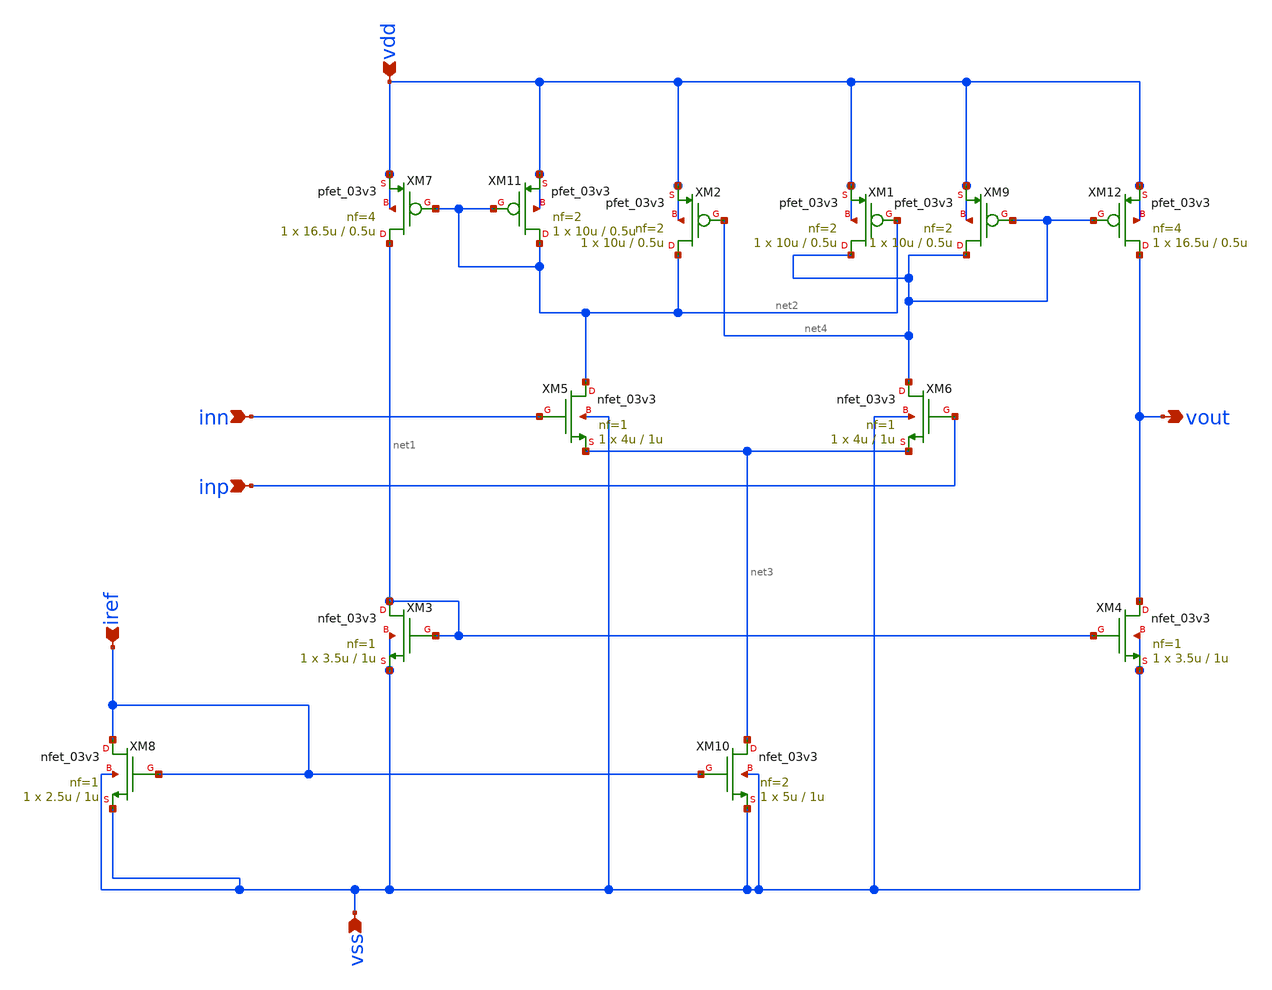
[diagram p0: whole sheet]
** sch_path: designs/libs/core_analog/Comparator/Nmos_Comparator.sch
**.subckt Nmos_Comparator vss vdd iref inn inp vout
*.ipin vss
*.ipin vdd
*.ipin iref
*.ipin inn
*.ipin inp
*.opin vout
XM3 net1 net1 vss vss nfet_03v3 L=1u W=3.5u nf=1 ad='int((nf+1)/2) * W/nf * 0.18u' as='int((nf+2)/2) * W/nf * 0.18u'
+ pd='2*int((nf+1)/2) * (W/nf + 0.18u)' ps='2*int((nf+2)/2) * (W/nf + 0.18u)' nrd='0.18u / W' nrs='0.18u / W'
+ sa=0 sb=0 sd=0 m=1
XM4 vout net1 vss vss nfet_03v3 L=1u W=3.5u nf=1 ad='int((nf+1)/2) * W/nf * 0.18u' as='int((nf+2)/2) * W/nf * 0.18u'
+ pd='2*int((nf+1)/2) * (W/nf + 0.18u)' ps='2*int((nf+2)/2) * (W/nf + 0.18u)' nrd='0.18u / W' nrs='0.18u / W'
+ sa=0 sb=0 sd=0 m=1
XM5 net2 inn net3 vss nfet_03v3 L=1u W=4u nf=1 ad='int((nf+1)/2) * W/nf * 0.18u' as='int((nf+2)/2) * W/nf * 0.18u'
+ pd='2*int((nf+1)/2) * (W/nf + 0.18u)' ps='2*int((nf+2)/2) * (W/nf + 0.18u)' nrd='0.18u / W' nrs='0.18u / W'
+ sa=0 sb=0 sd=0 m=1
XM6 net4 inp net3 vss nfet_03v3 L=1u W=4u nf=1 ad='int((nf+1)/2) * W/nf * 0.18u' as='int((nf+2)/2) * W/nf * 0.18u'
+ pd='2*int((nf+1)/2) * (W/nf + 0.18u)' ps='2*int((nf+2)/2) * (W/nf + 0.18u)' nrd='0.18u / W' nrs='0.18u / W'
+ sa=0 sb=0 sd=0 m=1
XM7 net1 net2 vdd vdd pfet_03v3 L=0.5u W=16.5u nf=4 ad='int((nf+1)/2) * W/nf * 0.18u' as='int((nf+2)/2) * W/nf * 0.18u'
+ pd='2*int((nf+1)/2) * (W/nf + 0.18u)' ps='2*int((nf+2)/2) * (W/nf + 0.18u)' nrd='0.18u / W' nrs='0.18u / W'
+ sa=0 sb=0 sd=0 m=1
XM9 net4 net4 vdd vdd pfet_03v3 L=0.5u W=10u nf=2 ad='int((nf+1)/2) * W/nf * 0.18u' as='int((nf+2)/2) * W/nf * 0.18u'
+ pd='2*int((nf+1)/2) * (W/nf + 0.18u)' ps='2*int((nf+2)/2) * (W/nf + 0.18u)' nrd='0.18u / W' nrs='0.18u / W'
+ sa=0 sb=0 sd=0 m=1
XM11 net2 net2 vdd vdd pfet_03v3 L=0.5u W=10u nf=2 ad='int((nf+1)/2) * W/nf * 0.18u' as='int((nf+2)/2) * W/nf * 0.18u'
+ pd='2*int((nf+1)/2) * (W/nf + 0.18u)' ps='2*int((nf+2)/2) * (W/nf + 0.18u)' nrd='0.18u / W' nrs='0.18u / W'
+ sa=0 sb=0 sd=0 m=1
XM12 vout net4 vdd vdd pfet_03v3 L=0.5u W=16.5u nf=4 ad='int((nf+1)/2) * W/nf * 0.18u' as='int((nf+2)/2) * W/nf * 0.18u'
+ pd='2*int((nf+1)/2) * (W/nf + 0.18u)' ps='2*int((nf+2)/2) * (W/nf + 0.18u)' nrd='0.18u / W' nrs='0.18u / W'
+ sa=0 sb=0 sd=0 m=1
XM1 net4 net2 vdd vdd pfet_03v3 L=0.5u W=10u nf=2 ad='int((nf+1)/2) * W/nf * 0.18u' as='int((nf+2)/2) * W/nf * 0.18u'
+ pd='2*int((nf+1)/2) * (W/nf + 0.18u)' ps='2*int((nf+2)/2) * (W/nf + 0.18u)' nrd='0.18u / W' nrs='0.18u / W'
+ sa=0 sb=0 sd=0 m=1
XM2 net2 net4 vdd vdd pfet_03v3 L=0.5u W=10u nf=2 ad='int((nf+1)/2) * W/nf * 0.18u' as='int((nf+2)/2) * W/nf * 0.18u'
+ pd='2*int((nf+1)/2) * (W/nf + 0.18u)' ps='2*int((nf+2)/2) * (W/nf + 0.18u)' nrd='0.18u / W' nrs='0.18u / W'
+ sa=0 sb=0 sd=0 m=1
XM8 iref iref vss vss nfet_03v3 L=1u W=2.5u nf=1 ad='int((nf+1)/2) * W/nf * 0.18u' as='int((nf+2)/2) * W/nf * 0.18u'
+ pd='2*int((nf+1)/2) * (W/nf + 0.18u)' ps='2*int((nf+2)/2) * (W/nf + 0.18u)' nrd='0.18u / W' nrs='0.18u / W'
+ sa=0 sb=0 sd=0 m=1
XM10 net3 iref vss vss nfet_03v3 L=1u W=5u nf=2 ad='int((nf+1)/2) * W/nf * 0.18u' as='int((nf+2)/2) * W/nf * 0.18u'
+ pd='2*int((nf+1)/2) * (W/nf + 0.18u)' ps='2*int((nf+2)/2) * (W/nf + 0.18u)' nrd='0.18u / W' nrs='0.18u / W'
+ sa=0 sb=0 sd=0 m=1
**.ends
.end
